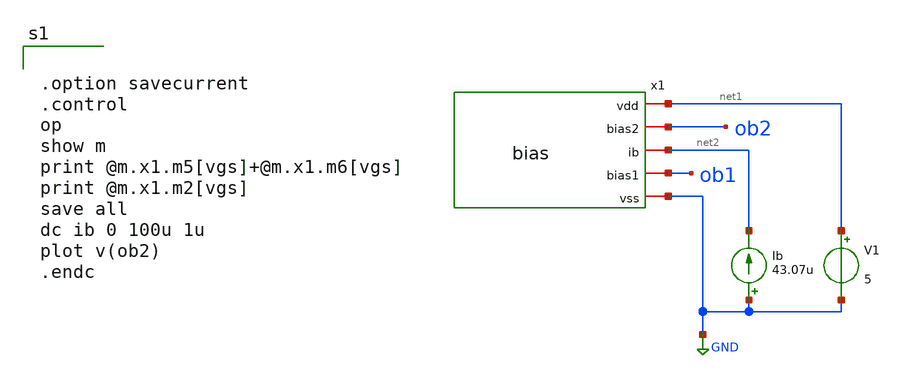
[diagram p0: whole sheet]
** sch_path: member_project/GroupWork/Team_masahiro/bias_dc.sch
**.subckt bias_dc
x1 net1 ob2 net2 ob1 GND bias
V1 net1 GND 5
Ib GND net2 43.07u
**** begin user architecture code
 .include $::LIB/mos.lib
.include $::LIB/passive.lib
.include $::LIB/diode.lib


.option savecurrent
.control
op
show m
print @m.x1.m5[vgs]+@m.x1.m6[vgs]
print @m.x1.m2[vgs]
save all
dc ib 0 100u 1u
plot v(ob2)
.endc


**** end user architecture code
**.ends

* expanding   symbol:  bias.sym # of pins=5
** sym_path: member_project/GroupWork/Team_masahiro/bias.sym
** sch_path: member_project/GroupWork/Team_masahiro/bias.sch
.subckt bias vdd bias2 ib bias1 vss
*.iopin ib
*.iopin vdd
*.iopin vss
*.iopin bias1
*.iopin bias2
M1 ib ib vss vss nmos L=2u W=20u m=1
M2 net1 ib vss vss nmos L=2u W=20u m=1
M3 net1 net1 vdd vdd pmos L=2u W=20u m=1
M4 bias2 net1 vdd vdd pmos L=2u W=20u m=1
M5 bias2 bias2 net2 vss nmos L=1u W=15u m=1
M6 net2 net2 vss vss nmos L=1u W=15u m=1
.ends

.GLOBAL GND
.end
